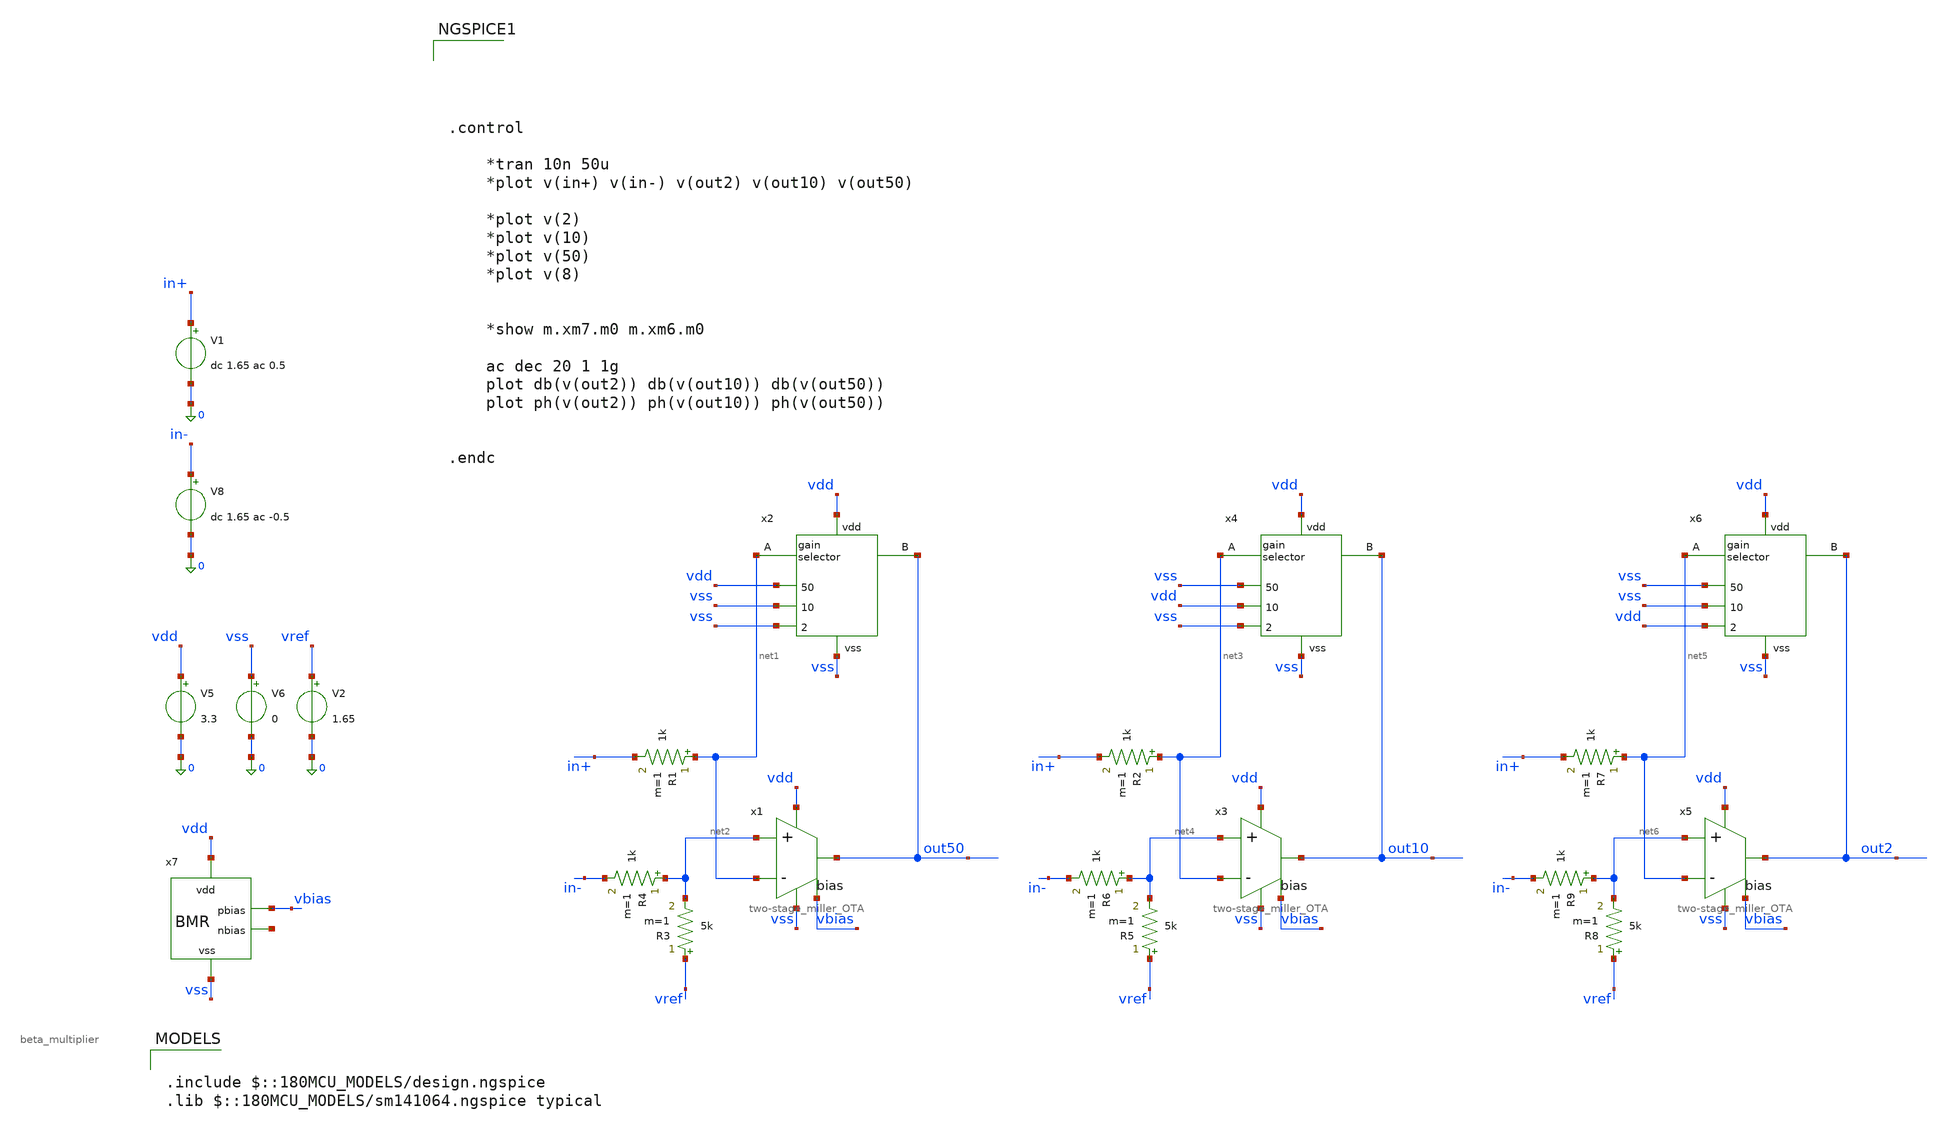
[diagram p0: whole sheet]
** sch_path: simulation/testbench_analog/PGA/PGA_freq_response.sch
**.subckt PGA_freq_response
V5 vdd 0 3.3
V6 vss 0 0
V8 in- 0 dc 1.65 ac -0.5
V1 in+ 0 dc 1.65 ac 0.5
R1 net1 in+ 1k m=1
V2 vref 0 1.65
R3 vref net2 5k m=1
R4 net2 in- 1k m=1
x1 vdd out50 net2 net1 vbias vss two-stage_miller_OTA
R2 net3 in+ 1k m=1
R5 vref net4 5k m=1
R6 net4 in- 1k m=1
x3 vdd out10 net4 net3 vbias vss two-stage_miller_OTA
R7 net5 in+ 1k m=1
R8 vref net6 5k m=1
R9 net6 in- 1k m=1
x5 vdd out2 net6 net5 vbias vss two-stage_miller_OTA
x2 vdd vss vdd net1 vss out50 vss gain_selector
x4 vdd vss vss net3 vdd out10 vss gain_selector
x6 vdd vss vss net5 vss out2 vdd gain_selector
x7 vdd vbias net7 vss beta_multiplier
**** begin user architecture code





.control

	*tran 10n 50u
	*plot v(in+) v(in-) v(out2) v(out10) v(out50)

	*plot v(2)
	*plot v(10)
	*plot v(50)
	*plot v(8)


	*show m.xm7.m0 m.xm6.m0

	ac dec 20 1 1g
	plot db(v(out2)) db(v(out10)) db(v(out50))
	plot ph(v(out2)) ph(v(out10)) ph(v(out50))


.endc



.include $::180MCU_MODELS/design.ngspice
.lib $::180MCU_MODELS/sm141064.ngspice typical

**** end user architecture code
**.ends

* expanding   symbol:  acoustic_ranger_2026/two-stage_miller_OTA.sym # of pins=6
** sym_path: design/analog/OTA/two-stage_miller_OTA.sym
** sch_path: design/analog/OTA/two-stage_miller_OTA.sch
.subckt two-stage_miller_OTA vdd out in+ in- bias vss
*.ipin in+
*.ipin in-
*.opin out
*.iopin vdd
*.iopin vss
*.ipin bias
XM1 net2 in- net1 vdd pfet_03v3 L=1u W=6.2u nf=1 ad='int((nf+1)/2) * W/nf * 0.18u' as='int((nf+2)/2) * W/nf * 0.18u'
+ pd='2*int((nf+1)/2) * (W/nf + 0.18u)' ps='2*int((nf+2)/2) * (W/nf + 0.18u)' nrd='0.18u / W' nrs='0.18u / W'
+ sa=0 sb=0 sd=0 m=8
XM2 net3 in+ net1 vdd pfet_03v3 L=1u W=6.2u nf=1 ad='int((nf+1)/2) * W/nf * 0.18u' as='int((nf+2)/2) * W/nf * 0.18u'
+ pd='2*int((nf+1)/2) * (W/nf + 0.18u)' ps='2*int((nf+2)/2) * (W/nf + 0.18u)' nrd='0.18u / W' nrs='0.18u / W'
+ sa=0 sb=0 sd=0 m=8
XM14 net3 net2 vss vss nfet_03v3 L=3u W=7.7u nf=4 ad='int((nf+1)/2) * W/nf * 0.18u' as='int((nf+2)/2) * W/nf * 0.18u'
+ pd='2*int((nf+1)/2) * (W/nf + 0.18u)' ps='2*int((nf+2)/2) * (W/nf + 0.18u)' nrd='0.18u / W' nrs='0.18u / W'
+ sa=0 sb=0 sd=0 m=2
XM15 net2 net2 vss vss nfet_03v3 L=3u W=7.7u nf=4 ad='int((nf+1)/2) * W/nf * 0.18u' as='int((nf+2)/2) * W/nf * 0.18u'
+ pd='2*int((nf+1)/2) * (W/nf + 0.18u)' ps='2*int((nf+2)/2) * (W/nf + 0.18u)' nrd='0.18u / W' nrs='0.18u / W'
+ sa=0 sb=0 sd=0 m=2
XM3 out net3 vss vss nfet_03v3 L=3u W=7.7u nf=4 ad='int((nf+1)/2) * W/nf * 0.18u' as='int((nf+2)/2) * W/nf * 0.18u'
+ pd='2*int((nf+1)/2) * (W/nf + 0.18u)' ps='2*int((nf+2)/2) * (W/nf + 0.18u)' nrd='0.18u / W' nrs='0.18u / W'
+ sa=0 sb=0 sd=0 m=12
C1 out net3 5p m=1
XM4 net1 bias vdd vdd pfet_03v3 L=20u W=25.3u nf=2 ad='int((nf+1)/2) * W/nf * 0.18u' as='int((nf+2)/2) * W/nf * 0.18u'
+ pd='2*int((nf+1)/2) * (W/nf + 0.18u)' ps='2*int((nf+2)/2) * (W/nf + 0.18u)' nrd='0.18u / W' nrs='0.18u / W'
+ sa=0 sb=0 sd=0 m=2
XM5 out bias vdd vdd pfet_03v3 L=20u W=25.3u nf=2 ad='int((nf+1)/2) * W/nf * 0.18u' as='int((nf+2)/2) * W/nf * 0.18u'
+ pd='2*int((nf+1)/2) * (W/nf + 0.18u)' ps='2*int((nf+2)/2) * (W/nf + 0.18u)' nrd='0.18u / W' nrs='0.18u / W'
+ sa=0 sb=0 sd=0 m=6
.ends


* expanding   symbol:  acoustic-ranger-dvl-processor/design/analog/PGA/gain_selector.sym # of pins=7
** sym_path: design/analog/PGA/gain_selector.sym
** sch_path: design/analog/PGA/gain_selector.sch
.subckt gain_selector vdd vss 50 A 10 B 2
*.iopin A
*.iopin B
*.ipin 2
*.ipin 10
*.ipin 50
*.iopin vdd
*.iopin vss
x9 A 2b 2 vdd vss net1 Transmission_Gate
R5 net1 B 2k m=1
x10 A 10b 10 vdd vss net2 Transmission_Gate
R6 net2 B 10k m=1
x11 A 50b 50 vdd vss net3 Transmission_Gate
R7 net3 B 50k m=1
XM9 50b 50 vdd vdd pfet_03v3 L=0.28u W=2u nf=1 ad='int((nf+1)/2) * W/nf * 0.18u' as='int((nf+2)/2) * W/nf * 0.18u'
+ pd='2*int((nf+1)/2) * (W/nf + 0.18u)' ps='2*int((nf+2)/2) * (W/nf + 0.18u)' nrd='0.18u / W' nrs='0.18u / W'
+ sa=0 sb=0 sd=0 m=1
XM10 50b 50 vss vss nfet_03v3 L=0.28u W=1u nf=1 ad='int((nf+1)/2) * W/nf * 0.18u' as='int((nf+2)/2) * W/nf * 0.18u'
+ pd='2*int((nf+1)/2) * (W/nf + 0.18u)' ps='2*int((nf+2)/2) * (W/nf + 0.18u)' nrd='0.18u / W' nrs='0.18u / W'
+ sa=0 sb=0 sd=0 m=1
XM11 10b 10 vdd vdd pfet_03v3 L=0.28u W=2u nf=1 ad='int((nf+1)/2) * W/nf * 0.18u' as='int((nf+2)/2) * W/nf * 0.18u'
+ pd='2*int((nf+1)/2) * (W/nf + 0.18u)' ps='2*int((nf+2)/2) * (W/nf + 0.18u)' nrd='0.18u / W' nrs='0.18u / W'
+ sa=0 sb=0 sd=0 m=1
XM12 10b 10 vss vss nfet_03v3 L=0.28u W=1u nf=1 ad='int((nf+1)/2) * W/nf * 0.18u' as='int((nf+2)/2) * W/nf * 0.18u'
+ pd='2*int((nf+1)/2) * (W/nf + 0.18u)' ps='2*int((nf+2)/2) * (W/nf + 0.18u)' nrd='0.18u / W' nrs='0.18u / W'
+ sa=0 sb=0 sd=0 m=1
XM13 2b 2 vdd vdd pfet_03v3 L=0.28u W=2u nf=1 ad='int((nf+1)/2) * W/nf * 0.18u' as='int((nf+2)/2) * W/nf * 0.18u'
+ pd='2*int((nf+1)/2) * (W/nf + 0.18u)' ps='2*int((nf+2)/2) * (W/nf + 0.18u)' nrd='0.18u / W' nrs='0.18u / W'
+ sa=0 sb=0 sd=0 m=1
XM14 2b 2 vss vss nfet_03v3 L=0.28u W=1u nf=1 ad='int((nf+1)/2) * W/nf * 0.18u' as='int((nf+2)/2) * W/nf * 0.18u'
+ pd='2*int((nf+1)/2) * (W/nf + 0.18u)' ps='2*int((nf+2)/2) * (W/nf + 0.18u)' nrd='0.18u / W' nrs='0.18u / W'
+ sa=0 sb=0 sd=0 m=1
.ends


* expanding   symbol:  acoustic-ranger-dvl-processor/design/analog/beta
*+ multiplier/beta_multiplier.sym # of pins=4
** sym_path: design/analog/beta multiplier/beta_multiplier.sym
** sch_path: design/analog/beta multiplier/beta_multiplier.sch
.subckt beta_multiplier vdd pbias nbias vss
*.iopin vdd
*.iopin vss
*.opin pbias
*.opin nbias
XM14 pbias nbias net1 net1 nfet_03v3 L=10u W=13.8u nf=1 ad='int((nf+1)/2) * W/nf * 0.18u' as='int((nf+2)/2) * W/nf * 0.18u'
+ pd='2*int((nf+1)/2) * (W/nf + 0.18u)' ps='2*int((nf+2)/2) * (W/nf + 0.18u)' nrd='0.18u / W' nrs='0.18u / W'
+ sa=0 sb=0 sd=0 m=1
XM15 nbias nbias vss vss nfet_03v3 L=10u W=5.71u nf=1 ad='int((nf+1)/2) * W/nf * 0.18u' as='int((nf+2)/2) * W/nf * 0.18u'
+ pd='2*int((nf+1)/2) * (W/nf + 0.18u)' ps='2*int((nf+2)/2) * (W/nf + 0.18u)' nrd='0.18u / W' nrs='0.18u / W'
+ sa=0 sb=0 sd=0 m=1
XM16 pbias pbias vdd vdd pfet_03v3 L=10u W=40u nf=1 ad='int((nf+1)/2) * W/nf * 0.18u' as='int((nf+2)/2) * W/nf * 0.18u'
+ pd='2*int((nf+1)/2) * (W/nf + 0.18u)' ps='2*int((nf+2)/2) * (W/nf + 0.18u)' nrd='0.18u / W' nrs='0.18u / W'
+ sa=0 sb=0 sd=0 m=1
XM17 nbias pbias vdd vdd pfet_03v3 L=10u W=40u nf=1 ad='int((nf+1)/2) * W/nf * 0.18u' as='int((nf+2)/2) * W/nf * 0.18u'
+ pd='2*int((nf+1)/2) * (W/nf + 0.18u)' ps='2*int((nf+2)/2) * (W/nf + 0.18u)' nrd='0.18u / W' nrs='0.18u / W'
+ sa=0 sb=0 sd=0 m=1
R3 net1 vss 9.012k m=1
.ends


* expanding   symbol:  Transmission_Gate.sym # of pins=6
** sym_path: design/analog/transmission_gate/Transmission_Gate.sym
** sch_path: design/analog/transmission_gate/Transmission_Gate.sch
.subckt Transmission_Gate A en_b en vdd vss B
*.ipin en_b
*.iopin A
*.iopin B
*.ipin en
*.iopin vdd
*.iopin vss
XM1 B en_b A vdd pfet_03v3 L=0.28u W=20u nf=10 ad='int((nf+1)/2) * W/nf * 0.18u' as='int((nf+2)/2) * W/nf * 0.18u'
+ pd='2*int((nf+1)/2) * (W/nf + 0.18u)' ps='2*int((nf+2)/2) * (W/nf + 0.18u)' nrd='0.18u / W' nrs='0.18u / W'
+ sa=0 sb=0 sd=0 m=8
XM2 A en B vss nfet_03v3 L=0.28u W=10u nf=5 ad='int((nf+1)/2) * W/nf * 0.18u' as='int((nf+2)/2) * W/nf * 0.18u'
+ pd='2*int((nf+1)/2) * (W/nf + 0.18u)' ps='2*int((nf+2)/2) * (W/nf + 0.18u)' nrd='0.18u / W' nrs='0.18u / W'
+ sa=0 sb=0 sd=0 m=8
.ends

.end
